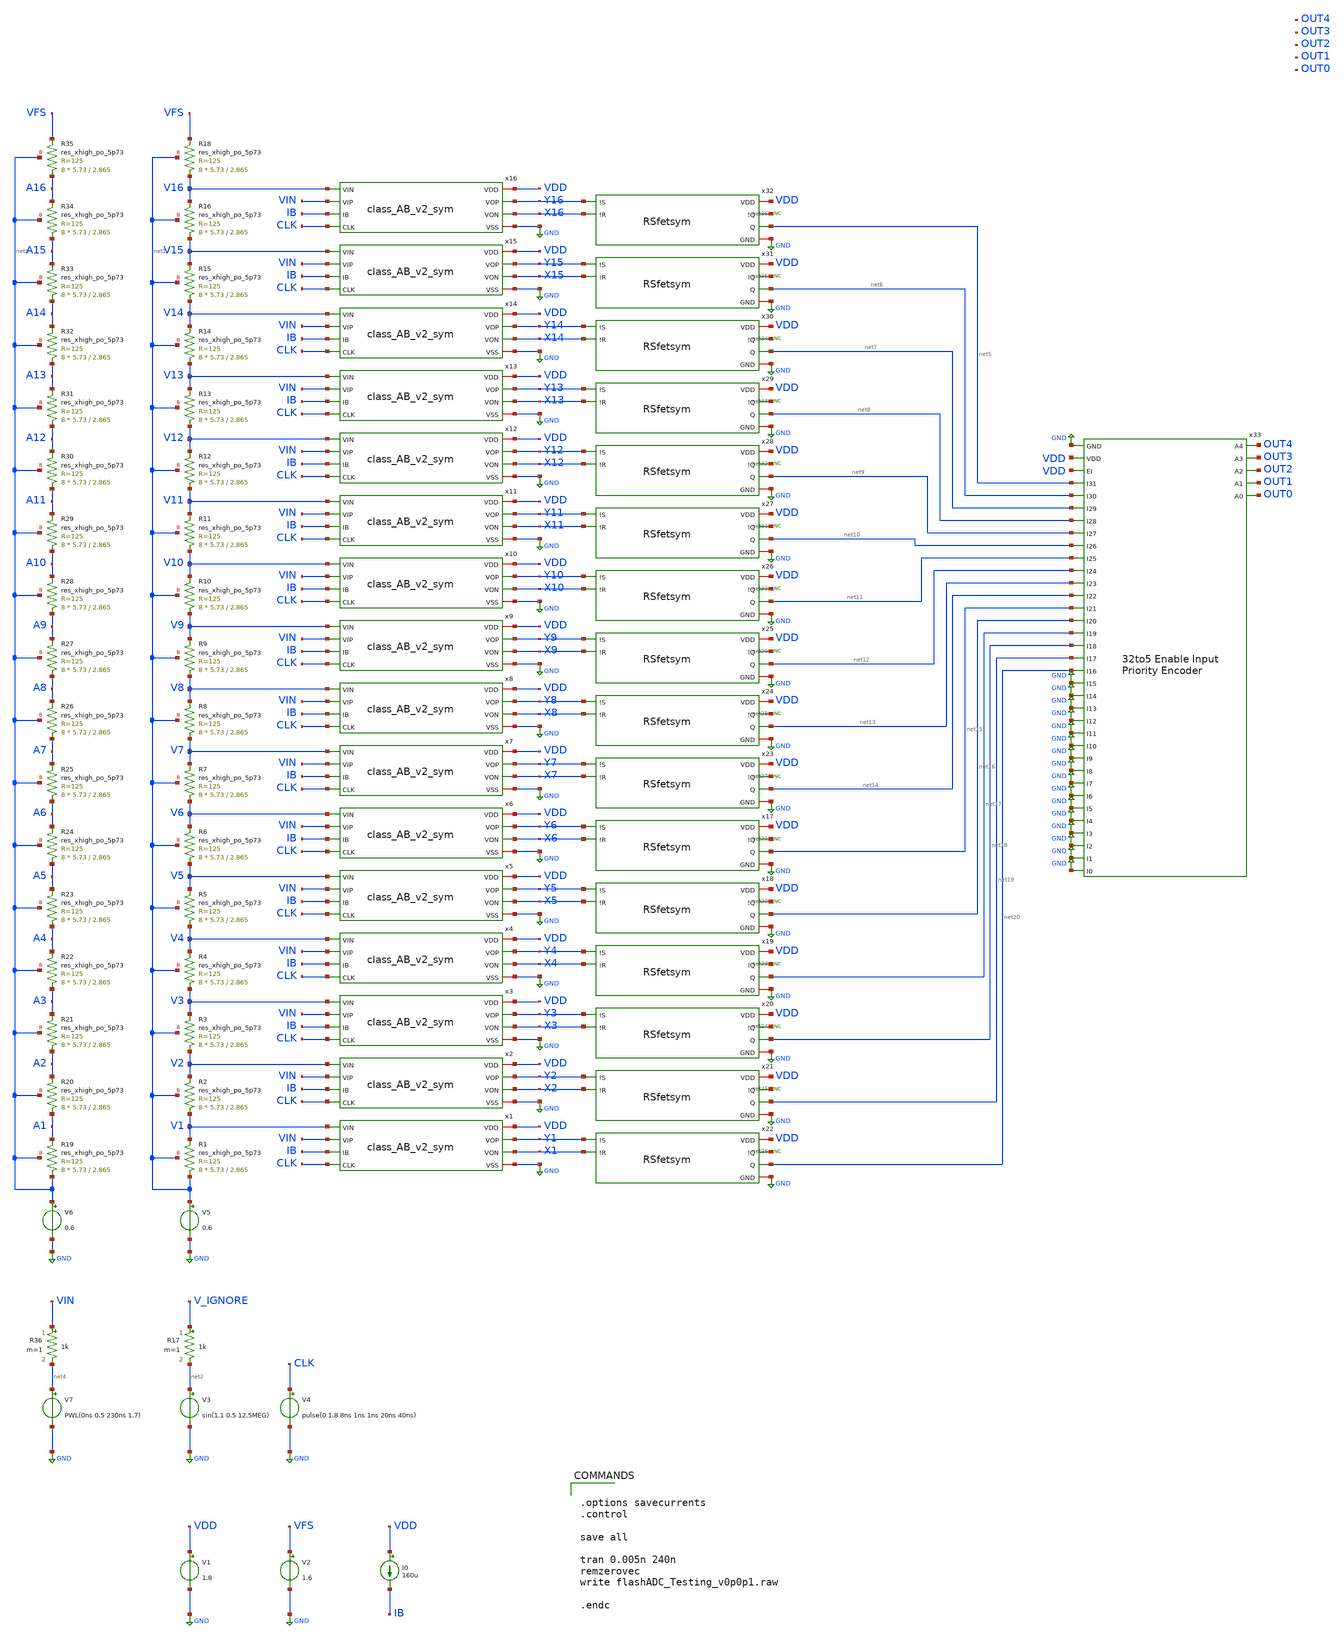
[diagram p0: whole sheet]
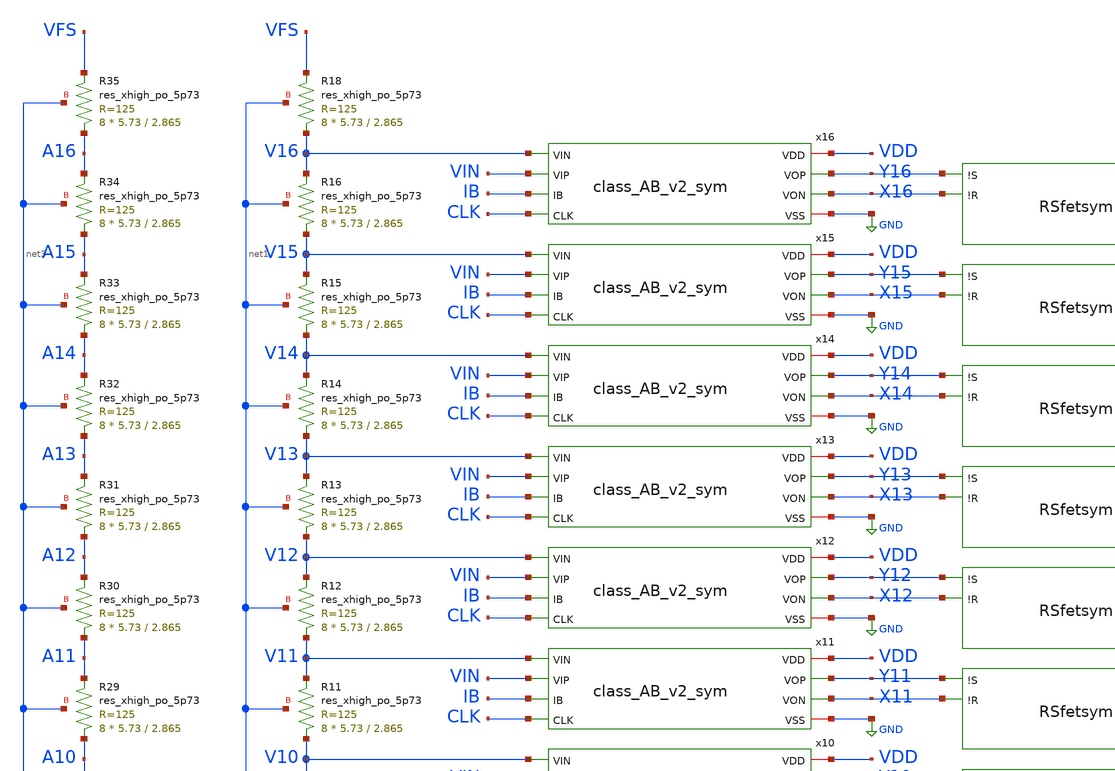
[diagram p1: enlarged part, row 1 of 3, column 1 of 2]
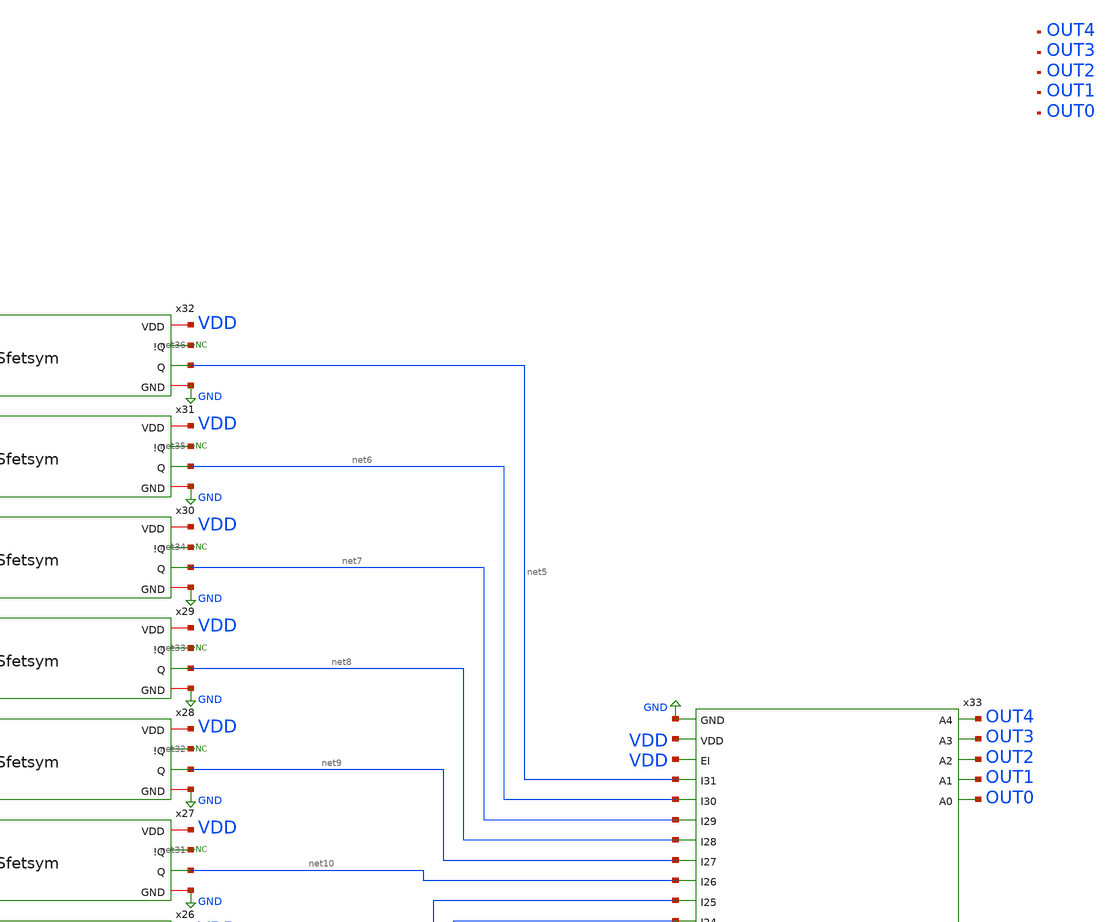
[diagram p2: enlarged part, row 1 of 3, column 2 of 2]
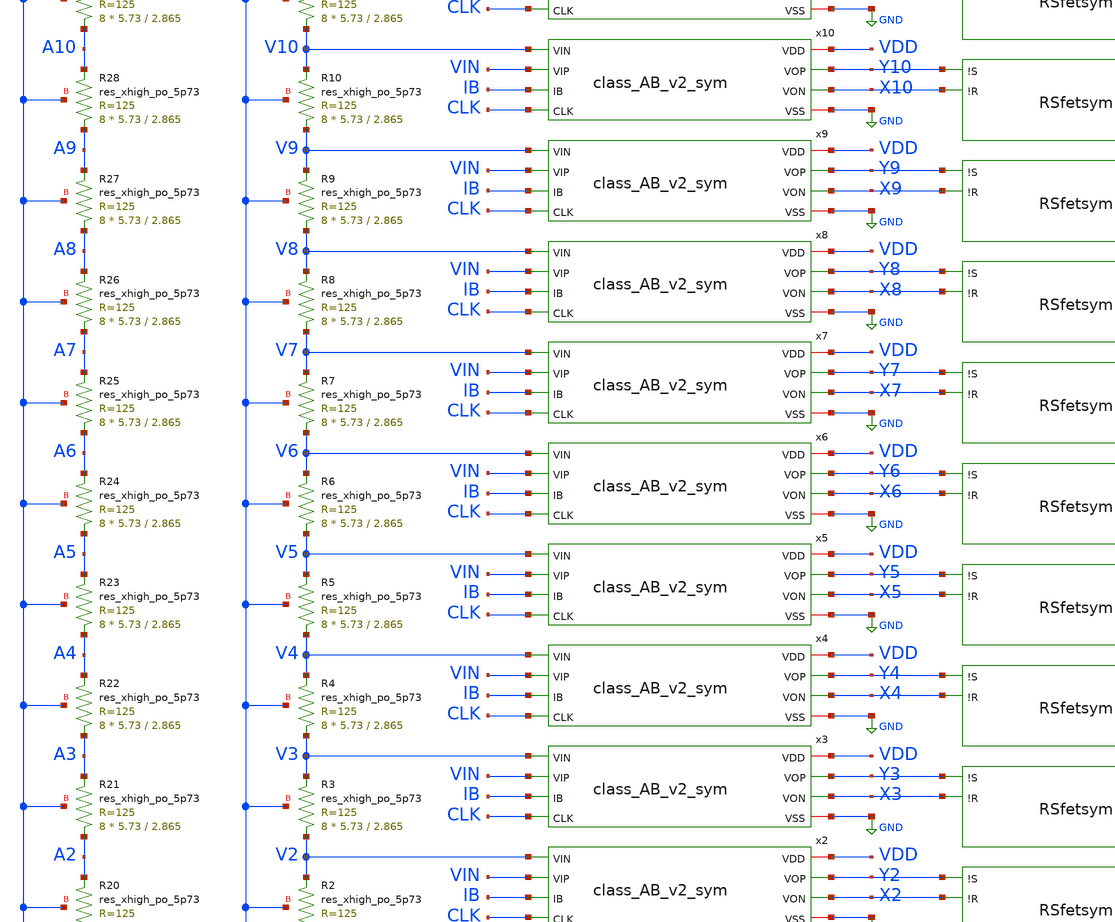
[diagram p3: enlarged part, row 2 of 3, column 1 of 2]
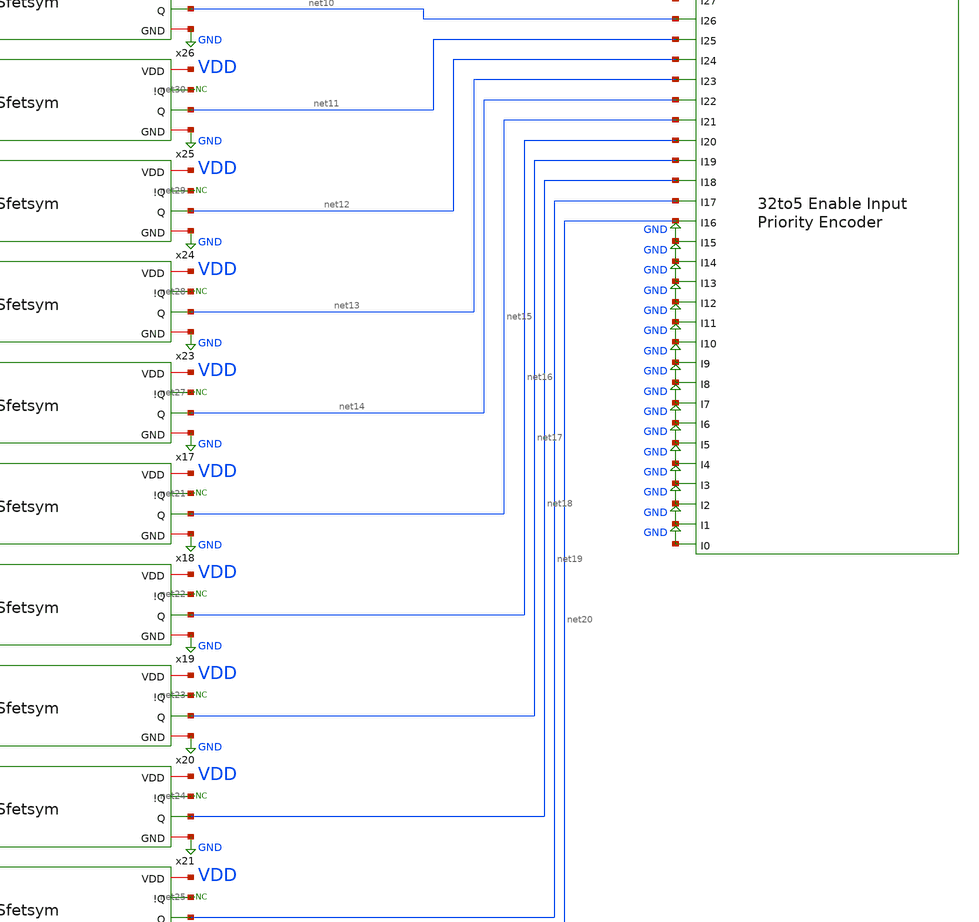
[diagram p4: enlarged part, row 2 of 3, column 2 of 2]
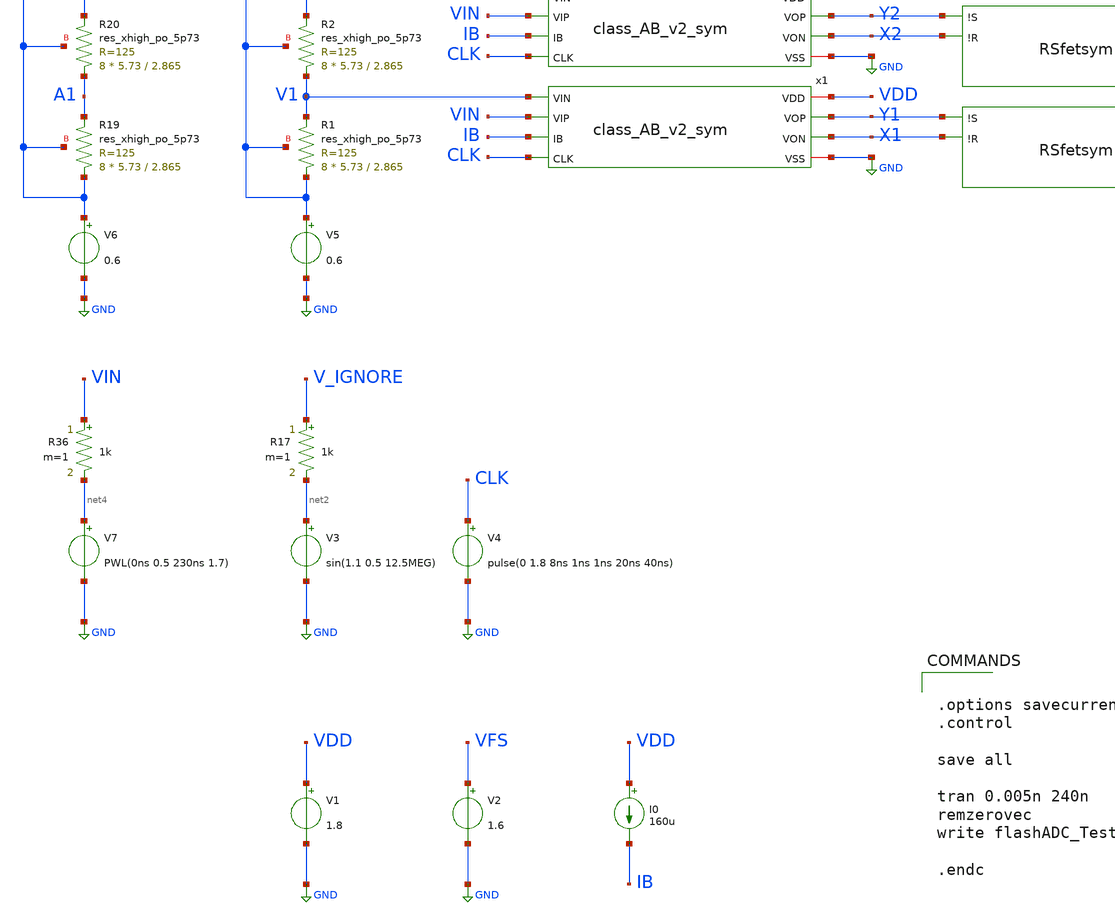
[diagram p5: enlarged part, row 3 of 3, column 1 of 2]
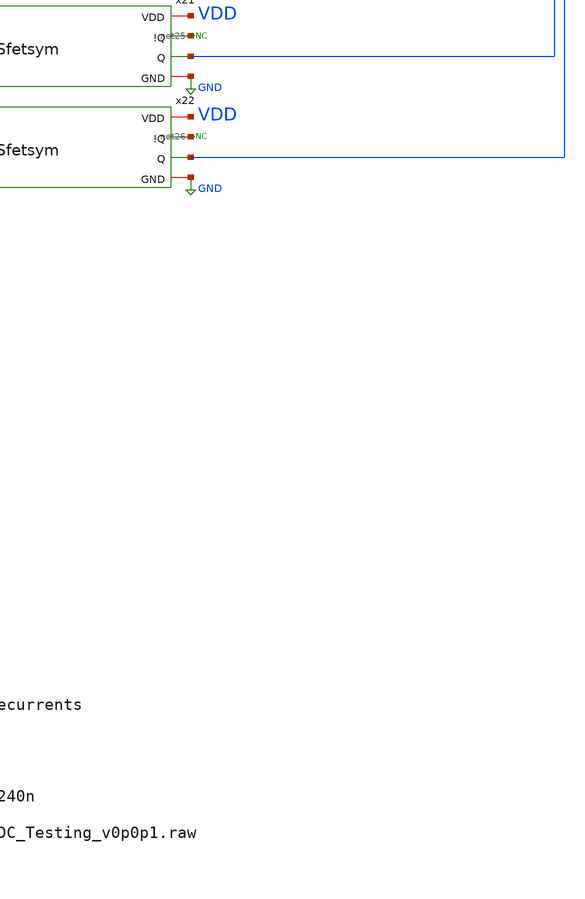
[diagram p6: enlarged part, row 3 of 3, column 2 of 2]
** sch_path: flashADC/flashADC_Testing_v0p0p1.sch
.lib $::SKYWATER_MODELS/sky130.lib.spice tt
.include $::SKYWATER_STDCELLS/sky130_fd_sc_hd.spice

**.subckt flashADC_Testing_v0p0p1
V3 net2 GND sin(1.1 0.5 12.5MEG)
V4 CLK GND pulse(0 1.8 8ns 1ns 1ns 20ns 40ns)
V1 VDD GND 1.8
V2 VFS GND 1.6
R17 V_IGNORE net2 1k m=1
I0 VDD IB 160u
V5 net1 GND 0.6
XR19 net3 A1 net3 sky130_fd_pr__res_xhigh_po_5p73 L=2.865 mult=8 m=8
V6 net3 GND 0.6
XR20 A1 A2 net3 sky130_fd_pr__res_xhigh_po_5p73 L=2.865 mult=8 m=8
XR21 A2 A3 net3 sky130_fd_pr__res_xhigh_po_5p73 L=2.865 mult=8 m=8
XR22 A3 A4 net3 sky130_fd_pr__res_xhigh_po_5p73 L=2.865 mult=8 m=8
XR23 A4 A5 net3 sky130_fd_pr__res_xhigh_po_5p73 L=2.865 mult=8 m=8
XR24 A5 A6 net3 sky130_fd_pr__res_xhigh_po_5p73 L=2.865 mult=8 m=8
XR25 A6 A7 net3 sky130_fd_pr__res_xhigh_po_5p73 L=2.865 mult=8 m=8
XR26 A7 A8 net3 sky130_fd_pr__res_xhigh_po_5p73 L=2.865 mult=8 m=8
XR27 A8 A9 net3 sky130_fd_pr__res_xhigh_po_5p73 L=2.865 mult=8 m=8
XR28 A9 A10 net3 sky130_fd_pr__res_xhigh_po_5p73 L=2.865 mult=8 m=8
XR29 A10 A11 net3 sky130_fd_pr__res_xhigh_po_5p73 L=2.865 mult=8 m=8
XR30 A11 A12 net3 sky130_fd_pr__res_xhigh_po_5p73 L=2.865 mult=8 m=8
XR31 A12 A13 net3 sky130_fd_pr__res_xhigh_po_5p73 L=2.865 mult=8 m=8
XR32 A13 A14 net3 sky130_fd_pr__res_xhigh_po_5p73 L=2.865 mult=8 m=8
XR33 A14 A15 net3 sky130_fd_pr__res_xhigh_po_5p73 L=2.865 mult=8 m=8
XR34 A15 A16 net3 sky130_fd_pr__res_xhigh_po_5p73 L=2.865 mult=8 m=8
XR35 A16 VFS net3 sky130_fd_pr__res_xhigh_po_5p73 L=2.865 mult=8 m=8
XR1 net1 V1 net1 sky130_fd_pr__res_xhigh_po_5p73 L=2.865 mult=8 m=8
XR2 V1 V2 net1 sky130_fd_pr__res_xhigh_po_5p73 L=2.865 mult=8 m=8
XR3 V2 V3 net1 sky130_fd_pr__res_xhigh_po_5p73 L=2.865 mult=8 m=8
XR4 V3 V4 net1 sky130_fd_pr__res_xhigh_po_5p73 L=2.865 mult=8 m=8
XR5 V4 V5 net1 sky130_fd_pr__res_xhigh_po_5p73 L=2.865 mult=8 m=8
XR6 V5 V6 net1 sky130_fd_pr__res_xhigh_po_5p73 L=2.865 mult=8 m=8
XR7 V6 V7 net1 sky130_fd_pr__res_xhigh_po_5p73 L=2.865 mult=8 m=8
XR8 V7 V8 net1 sky130_fd_pr__res_xhigh_po_5p73 L=2.865 mult=8 m=8
XR9 V8 V9 net1 sky130_fd_pr__res_xhigh_po_5p73 L=2.865 mult=8 m=8
XR10 V9 V10 net1 sky130_fd_pr__res_xhigh_po_5p73 L=2.865 mult=8 m=8
XR11 V10 V11 net1 sky130_fd_pr__res_xhigh_po_5p73 L=2.865 mult=8 m=8
XR12 V11 V12 net1 sky130_fd_pr__res_xhigh_po_5p73 L=2.865 mult=8 m=8
XR13 V12 V13 net1 sky130_fd_pr__res_xhigh_po_5p73 L=2.865 mult=8 m=8
XR14 V13 V14 net1 sky130_fd_pr__res_xhigh_po_5p73 L=2.865 mult=8 m=8
XR15 V14 V15 net1 sky130_fd_pr__res_xhigh_po_5p73 L=2.865 mult=8 m=8
XR16 V15 V16 net1 sky130_fd_pr__res_xhigh_po_5p73 L=2.865 mult=8 m=8
XR18 V16 VFS net1 sky130_fd_pr__res_xhigh_po_5p73 L=2.865 mult=8 m=8
V7 net4 GND PWL(0ns 0.5 230ns 1.7)
R36 VIN net4 1k m=1
x1 VDD Y1 X1 V1 VIN IB CLK GND class_AB_v2_sym
x2 VDD Y2 X2 V2 VIN IB CLK GND class_AB_v2_sym
x3 VDD Y3 X3 V3 VIN IB CLK GND class_AB_v2_sym
x4 VDD Y4 X4 V4 VIN IB CLK GND class_AB_v2_sym
x5 VDD Y5 X5 V5 VIN IB CLK GND class_AB_v2_sym
x6 VDD Y6 X6 V6 VIN IB CLK GND class_AB_v2_sym
x7 VDD Y7 X7 V7 VIN IB CLK GND class_AB_v2_sym
x8 VDD Y8 X8 V8 VIN IB CLK GND class_AB_v2_sym
x9 VDD Y9 X9 V9 VIN IB CLK GND class_AB_v2_sym
x10 VDD Y10 X10 V10 VIN IB CLK GND class_AB_v2_sym
x11 VDD Y11 X11 V11 VIN IB CLK GND class_AB_v2_sym
x12 VDD Y12 X12 V12 VIN IB CLK GND class_AB_v2_sym
x13 VDD Y13 X13 V13 VIN IB CLK GND class_AB_v2_sym
x14 VDD Y14 X14 V14 VIN IB CLK GND class_AB_v2_sym
x15 VDD Y15 X15 V15 VIN IB CLK GND class_AB_v2_sym
x16 VDD Y16 X16 V16 VIN IB CLK GND class_AB_v2_sym
x17 VDD Y6 X6 net21 net15 GND RSfetsym
x18 VDD Y5 X5 net22 net16 GND RSfetsym
x19 VDD Y4 X4 net23 net17 GND RSfetsym
x20 VDD Y3 X3 net24 net18 GND RSfetsym
x21 VDD Y2 X2 net25 net19 GND RSfetsym
x22 VDD Y1 X1 net26 net20 GND RSfetsym
x23 VDD Y7 X7 net27 net14 GND RSfetsym
x24 VDD Y8 X8 net28 net13 GND RSfetsym
x25 VDD Y9 X9 net29 net12 GND RSfetsym
x26 VDD Y10 X10 net30 net11 GND RSfetsym
x27 VDD Y11 X11 net31 net10 GND RSfetsym
x28 VDD Y12 X12 net32 net9 GND RSfetsym
x29 VDD Y13 X13 net33 net8 GND RSfetsym
x30 VDD Y14 X14 net34 net7 GND RSfetsym
x31 VDD Y15 X15 net35 net6 GND RSfetsym
x32 VDD Y16 X16 net36 net5 GND RSfetsym
x33 GND VDD VDD OUT4 net5 net6 net7 net8 net9 net10 net11 net12 OUT3 net13 net14 net15 net16 net17
+ net18 net19 net20 OUT2 GND GND GND GND GND GND GND OUT1 GND GND GND GND GND OUT0 GND GND GND GND
+ 32to5_Priority_Encoder_v0p2p1
* noconn #net26
* noconn #net25
* noconn #net24
* noconn #net23
* noconn #net22
* noconn #net21
* noconn #net27
* noconn #net28
* noconn #net29
* noconn #net30
* noconn #net31
* noconn #net32
* noconn #net33
* noconn #net34
* noconn #net35
* noconn #net36
**** begin user architecture code


.options savecurrents
.control

save all

tran 0.005n 240n
remzerovec
write flashADC_Testing_v0p0p1.raw

.endc


**** end user architecture code
**.ends
.GLOBAL GND
.end
